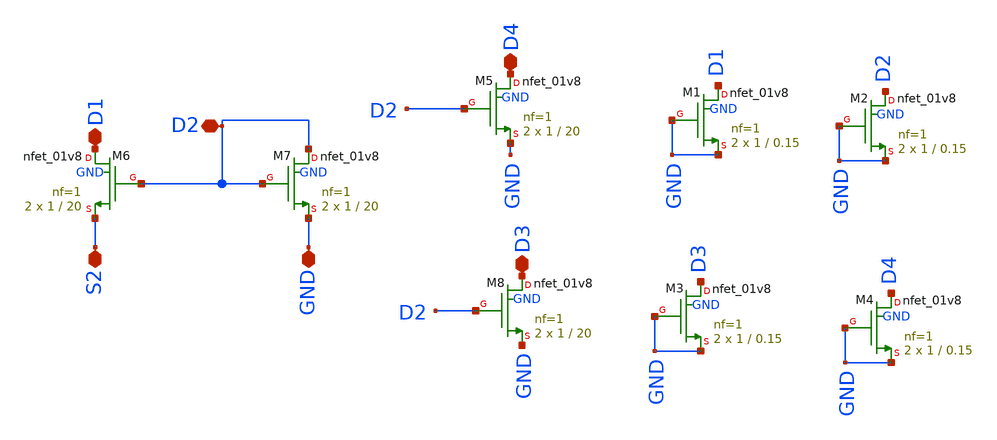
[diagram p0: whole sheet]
** sch_path: magic/nmos_tail_current_a.sch
**.subckt nmos_tail_current_a D1 S2 GND D2 D3 D4
*.iopin D1
*.iopin S2
*.iopin GND
*.iopin D2
*.iopin D3
*.iopin D4
XM8 D3 D2 GND GND sky130_fd_pr__nfet_01v8 L=20 W=1 nf=1 ad='int((nf+1)/2) * W/nf * 0.29' as='int((nf+2)/2) * W/nf * 0.29'
+ pd='2*int((nf+1)/2) * (W/nf + 0.29)' ps='2*int((nf+2)/2) * (W/nf + 0.29)' nrd='0.29 / W' nrs='0.29 / W'
+ sa=0 sb=0 sd=0 mult=2 m=2
XM6 D1 D2 S2 GND sky130_fd_pr__nfet_01v8 L=20 W=1 nf=1 ad='int((nf+1)/2) * W/nf * 0.29' as='int((nf+2)/2) * W/nf * 0.29'
+ pd='2*int((nf+1)/2) * (W/nf + 0.29)' ps='2*int((nf+2)/2) * (W/nf + 0.29)' nrd='0.29 / W' nrs='0.29 / W'
+ sa=0 sb=0 sd=0 mult=2 m=2
XM7 D2 D2 GND GND sky130_fd_pr__nfet_01v8 L=20 W=1 nf=1 ad='int((nf+1)/2) * W/nf * 0.29' as='int((nf+2)/2) * W/nf * 0.29'
+ pd='2*int((nf+1)/2) * (W/nf + 0.29)' ps='2*int((nf+2)/2) * (W/nf + 0.29)' nrd='0.29 / W' nrs='0.29 / W'
+ sa=0 sb=0 sd=0 mult=2 m=2
XM5 D4 D2 GND GND sky130_fd_pr__nfet_01v8 L=20 W=1 nf=1 ad='int((nf+1)/2) * W/nf * 0.29' as='int((nf+2)/2) * W/nf * 0.29'
+ pd='2*int((nf+1)/2) * (W/nf + 0.29)' ps='2*int((nf+2)/2) * (W/nf + 0.29)' nrd='0.29 / W' nrs='0.29 / W'
+ sa=0 sb=0 sd=0 mult=2 m=2
XM1 D1 GND GND GND sky130_fd_pr__nfet_01v8 L=0.15 W=1 nf=1 ad='int((nf+1)/2) * W/nf * 0.29' as='int((nf+2)/2) * W/nf * 0.29'
+ pd='2*int((nf+1)/2) * (W/nf + 0.29)' ps='2*int((nf+2)/2) * (W/nf + 0.29)' nrd='0.29 / W' nrs='0.29 / W'
+ sa=0 sb=0 sd=0 mult=2 m=2
XM2 D2 GND GND GND sky130_fd_pr__nfet_01v8 L=0.15 W=1 nf=1 ad='int((nf+1)/2) * W/nf * 0.29' as='int((nf+2)/2) * W/nf * 0.29'
+ pd='2*int((nf+1)/2) * (W/nf + 0.29)' ps='2*int((nf+2)/2) * (W/nf + 0.29)' nrd='0.29 / W' nrs='0.29 / W'
+ sa=0 sb=0 sd=0 mult=2 m=2
XM3 D3 GND GND GND sky130_fd_pr__nfet_01v8 L=0.15 W=1 nf=1 ad='int((nf+1)/2) * W/nf * 0.29' as='int((nf+2)/2) * W/nf * 0.29'
+ pd='2*int((nf+1)/2) * (W/nf + 0.29)' ps='2*int((nf+2)/2) * (W/nf + 0.29)' nrd='0.29 / W' nrs='0.29 / W'
+ sa=0 sb=0 sd=0 mult=2 m=2
XM4 D4 GND GND GND sky130_fd_pr__nfet_01v8 L=0.15 W=1 nf=1 ad='int((nf+1)/2) * W/nf * 0.29' as='int((nf+2)/2) * W/nf * 0.29'
+ pd='2*int((nf+1)/2) * (W/nf + 0.29)' ps='2*int((nf+2)/2) * (W/nf + 0.29)' nrd='0.29 / W' nrs='0.29 / W'
+ sa=0 sb=0 sd=0 mult=2 m=2
**.ends
.end
